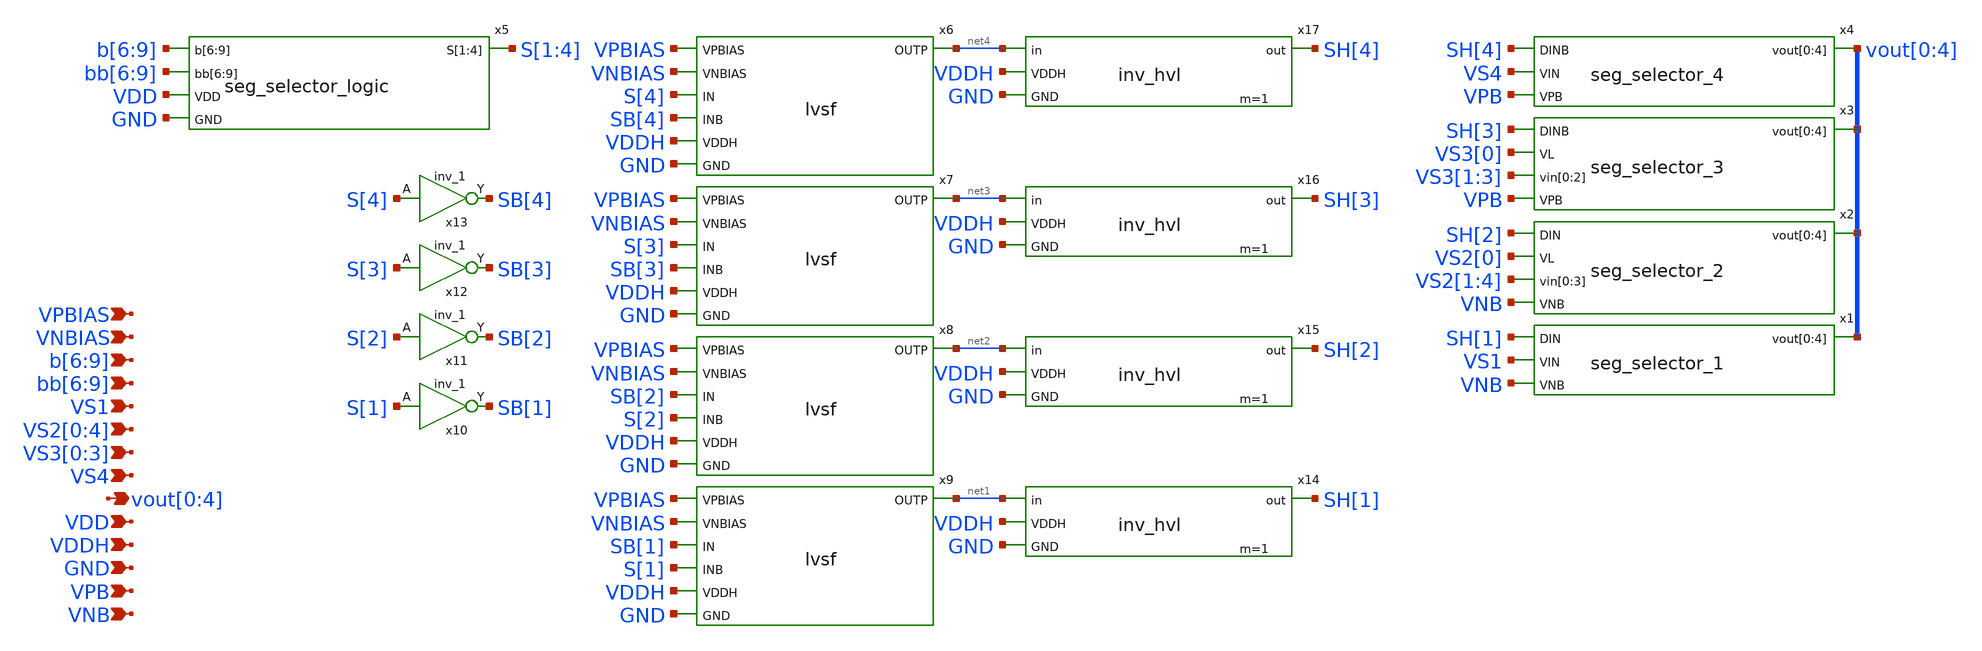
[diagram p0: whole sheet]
** sch_path: xschem/seg_selector.sch
**.subckt seg_selector vout[0],vout[1],vout[2],vout[3],vout[4] VNB VPB b[6],b[7],b[8],b[9] VS1
*+ VS2[0],VS2[1],VS2[2],VS2[3],VS2[4] VS3[0],VS3[1],VS3[2],VS3[3] VS4 bb[6],bb[7],bb[8],bb[9] GND VDD VPBIAS VNBIAS VDDH
*.opin vout[0],vout[1],vout[2],vout[3],vout[4]
*.ipin VNB
*.ipin VPB
*.ipin b[6],b[7],b[8],b[9]
*.ipin VS1
*.ipin VS2[0],VS2[1],VS2[2],VS2[3],VS2[4]
*.ipin VS3[0],VS3[1],VS3[2],VS3[3]
*.ipin VS4
*.ipin bb[6],bb[7],bb[8],bb[9]
*.ipin GND
*.ipin VDD
*.ipin VPBIAS
*.ipin VNBIAS
*.ipin VDDH
x1 SH[1] VS1 vout[0] vout[1] vout[2] vout[3] vout[4] VNB seg_selector_1
x2 SH[2] VS2[0] VS2[1] VS2[2] VS2[3] VS2[4] vout[0] vout[1] vout[2] vout[3] vout[4] VNB
+ seg_selector_2
x3 SH[3] VS3[0] VS3[1] VS3[2] VS3[3] vout[0] vout[1] vout[2] vout[3] vout[4] VPB seg_selector_3
x4 SH[4] VS4 vout[0] vout[1] vout[2] vout[3] vout[4] VPB seg_selector_4
x5 b[6] b[7] b[8] b[9] bb[6] bb[7] bb[8] bb[9] S[1] S[2] S[3] S[4] VDD GND seg_selector_logic
x6 VPBIAS VNBIAS S[4] SB[4] net4 VDDH GND lvsf
x7 VPBIAS VNBIAS S[3] SB[3] net3 VDDH GND lvsf
x8 VPBIAS VNBIAS SB[2] S[2] net2 VDDH GND lvsf
x9 VPBIAS VNBIAS SB[1] S[1] net1 VDDH GND lvsf
x10 S[1] GND GND VDD VDD SB[1] sky130_fd_sc_hd__inv_1
x11 S[2] GND GND VDD VDD SB[2] sky130_fd_sc_hd__inv_1
x12 S[3] GND GND VDD VDD SB[3] sky130_fd_sc_hd__inv_1
x13 S[4] GND GND VDD VDD SB[4] sky130_fd_sc_hd__inv_1
x14 net1 SH[1] VDDH GND inv_hvl m=1
x15 net2 SH[2] VDDH GND inv_hvl m=1
x16 net3 SH[3] VDDH GND inv_hvl m=1
x17 net4 SH[4] VDDH GND inv_hvl m=1
**.ends

* expanding   symbol:  seg_selector_1.sym # of pins=4
** sym_path: xschem/seg_selector_1.sym
** sch_path: xschem/seg_selector_1.sch
.subckt seg_selector_1 DIN VIN vout[0] vout[1] vout[2] vout[3] vout[4] VNB
*.opin vout[0],vout[1],vout[2],vout[3],vout[4]
*.ipin VNB
*.ipin DIN
*.ipin VIN
.param wp=0.42 wn=0.42 l=0.5

XM1 vout[0] DIN VIN VNB sky130_fd_pr__nfet_g5v0d10v5 L=l W=wn nf=1 ad='int((nf+1)/2) * W/nf * 0.29' as='int((nf+2)/2) * W/nf * 0.29'
+ pd='2*int((nf+1)/2) * (W/nf + 0.29)' ps='2*int((nf+2)/2) * (W/nf + 0.29)' nrd='0.29 / W' nrs='0.29 / W'
+ sa=0 sb=0 sd=0 mult=1 m=1
XM2 vout[1] DIN VIN VNB sky130_fd_pr__nfet_g5v0d10v5 L=l W=wn nf=1 ad='int((nf+1)/2) * W/nf * 0.29' as='int((nf+2)/2) * W/nf * 0.29'
+ pd='2*int((nf+1)/2) * (W/nf + 0.29)' ps='2*int((nf+2)/2) * (W/nf + 0.29)' nrd='0.29 / W' nrs='0.29 / W'
+ sa=0 sb=0 sd=0 mult=1 m=1
XM3 vout[2] DIN VIN VNB sky130_fd_pr__nfet_g5v0d10v5 L=l W=wn nf=1 ad='int((nf+1)/2) * W/nf * 0.29' as='int((nf+2)/2) * W/nf * 0.29'
+ pd='2*int((nf+1)/2) * (W/nf + 0.29)' ps='2*int((nf+2)/2) * (W/nf + 0.29)' nrd='0.29 / W' nrs='0.29 / W'
+ sa=0 sb=0 sd=0 mult=1 m=1
XM4 vout[3] DIN VIN VNB sky130_fd_pr__nfet_g5v0d10v5 L=l W=wn nf=1 ad='int((nf+1)/2) * W/nf * 0.29' as='int((nf+2)/2) * W/nf * 0.29'
+ pd='2*int((nf+1)/2) * (W/nf + 0.29)' ps='2*int((nf+2)/2) * (W/nf + 0.29)' nrd='0.29 / W' nrs='0.29 / W'
+ sa=0 sb=0 sd=0 mult=1 m=1
XM5 vout[4] DIN VIN VNB sky130_fd_pr__nfet_g5v0d10v5 L=l W=wn nf=1 ad='int((nf+1)/2) * W/nf * 0.29' as='int((nf+2)/2) * W/nf * 0.29'
+ pd='2*int((nf+1)/2) * (W/nf + 0.29)' ps='2*int((nf+2)/2) * (W/nf + 0.29)' nrd='0.29 / W' nrs='0.29 / W'
+ sa=0 sb=0 sd=0 mult=1 m=1
.ends


* expanding   symbol:  seg_selector_2.sym # of pins=5
** sym_path: xschem/seg_selector_2.sym
** sch_path: xschem/seg_selector_2.sch
.subckt seg_selector_2 DIN VL vin[0] vin[1] vin[2] vin[3] vout[0] vout[1] vout[2] vout[3] vout[4]
+ VNB
*.opin vout[0],vout[1],vout[2],vout[3],vout[4]
*.ipin VNB
*.ipin DIN
*.ipin vin[0],vin[1],vin[2],vin[3]
*.ipin VL
.param wp=0.42 wn=0.42 l=0.5

XM1 vout[0] DIN VL VNB sky130_fd_pr__nfet_g5v0d10v5 L=l W=wn nf=1 ad='int((nf+1)/2) * W/nf * 0.29' as='int((nf+2)/2) * W/nf * 0.29'
+ pd='2*int((nf+1)/2) * (W/nf + 0.29)' ps='2*int((nf+2)/2) * (W/nf + 0.29)' nrd='0.29 / W' nrs='0.29 / W'
+ sa=0 sb=0 sd=0 mult=1 m=1
XM2 vout[1] DIN vin[0] VNB sky130_fd_pr__nfet_g5v0d10v5 L=l W=wn nf=1 ad='int((nf+1)/2) * W/nf * 0.29'
+ as='int((nf+2)/2) * W/nf * 0.29' pd='2*int((nf+1)/2) * (W/nf + 0.29)' ps='2*int((nf+2)/2) * (W/nf + 0.29)'
+ nrd='0.29 / W' nrs='0.29 / W' sa=0 sb=0 sd=0 mult=1 m=1
XM3 vout[2] DIN vin[1] VNB sky130_fd_pr__nfet_g5v0d10v5 L=l W=wn nf=1 ad='int((nf+1)/2) * W/nf * 0.29'
+ as='int((nf+2)/2) * W/nf * 0.29' pd='2*int((nf+1)/2) * (W/nf + 0.29)' ps='2*int((nf+2)/2) * (W/nf + 0.29)'
+ nrd='0.29 / W' nrs='0.29 / W' sa=0 sb=0 sd=0 mult=1 m=1
XM4 vout[3] DIN vin[2] VNB sky130_fd_pr__nfet_g5v0d10v5 L=l W=wn nf=1 ad='int((nf+1)/2) * W/nf * 0.29'
+ as='int((nf+2)/2) * W/nf * 0.29' pd='2*int((nf+1)/2) * (W/nf + 0.29)' ps='2*int((nf+2)/2) * (W/nf + 0.29)'
+ nrd='0.29 / W' nrs='0.29 / W' sa=0 sb=0 sd=0 mult=1 m=1
XM5 vout[4] DIN vin[3] VNB sky130_fd_pr__nfet_g5v0d10v5 L=l W=wn nf=1 ad='int((nf+1)/2) * W/nf * 0.29'
+ as='int((nf+2)/2) * W/nf * 0.29' pd='2*int((nf+1)/2) * (W/nf + 0.29)' ps='2*int((nf+2)/2) * (W/nf + 0.29)'
+ nrd='0.29 / W' nrs='0.29 / W' sa=0 sb=0 sd=0 mult=1 m=1
.ends


* expanding   symbol:  seg_selector_3.sym # of pins=5
** sym_path: xschem/seg_selector_3.sym
** sch_path: xschem/seg_selector_3.sch
.subckt seg_selector_3 DINB VL vin[0] vin[1] vin[2] vout[0] vout[1] vout[2] vout[3] vout[4] VPB
*.opin vout[0],vout[1],vout[2],vout[3],vout[4]
*.ipin VPB
*.ipin DINB
*.ipin vin[0],vin[1],vin[2]
*.ipin VL
.param wp=0.42 wn=0.42 l=0.5

XM1 vout[0] DINB VL VPB sky130_fd_pr__pfet_g5v0d10v5 L=l W=wp nf=1 ad='int((nf+1)/2) * W/nf * 0.29' as='int((nf+2)/2) * W/nf * 0.29'
+ pd='2*int((nf+1)/2) * (W/nf + 0.29)' ps='2*int((nf+2)/2) * (W/nf + 0.29)' nrd='0.29 / W' nrs='0.29 / W'
+ sa=0 sb=0 sd=0 mult=1 m=1
XM2 vout[1] DINB VL VPB sky130_fd_pr__pfet_g5v0d10v5 L=l W=wp nf=1 ad='int((nf+1)/2) * W/nf * 0.29' as='int((nf+2)/2) * W/nf * 0.29'
+ pd='2*int((nf+1)/2) * (W/nf + 0.29)' ps='2*int((nf+2)/2) * (W/nf + 0.29)' nrd='0.29 / W' nrs='0.29 / W'
+ sa=0 sb=0 sd=0 mult=1 m=1
XM3 vout[2] DINB vin[0] VPB sky130_fd_pr__pfet_g5v0d10v5 L=l W=wp nf=1 ad='int((nf+1)/2) * W/nf * 0.29'
+ as='int((nf+2)/2) * W/nf * 0.29' pd='2*int((nf+1)/2) * (W/nf + 0.29)' ps='2*int((nf+2)/2) * (W/nf + 0.29)'
+ nrd='0.29 / W' nrs='0.29 / W' sa=0 sb=0 sd=0 mult=1 m=1
XM4 vout[3] DINB vin[1] VPB sky130_fd_pr__pfet_g5v0d10v5 L=l W=wp nf=1 ad='int((nf+1)/2) * W/nf * 0.29'
+ as='int((nf+2)/2) * W/nf * 0.29' pd='2*int((nf+1)/2) * (W/nf + 0.29)' ps='2*int((nf+2)/2) * (W/nf + 0.29)'
+ nrd='0.29 / W' nrs='0.29 / W' sa=0 sb=0 sd=0 mult=1 m=1
XM5 vout[4] DINB vin[2] VPB sky130_fd_pr__pfet_g5v0d10v5 L=l W=wp nf=1 ad='int((nf+1)/2) * W/nf * 0.29'
+ as='int((nf+2)/2) * W/nf * 0.29' pd='2*int((nf+1)/2) * (W/nf + 0.29)' ps='2*int((nf+2)/2) * (W/nf + 0.29)'
+ nrd='0.29 / W' nrs='0.29 / W' sa=0 sb=0 sd=0 mult=1 m=1
.ends


* expanding   symbol:  seg_selector_4.sym # of pins=4
** sym_path: xschem/seg_selector_4.sym
** sch_path: xschem/seg_selector_4.sch
.subckt seg_selector_4 DINB VIN vout[0] vout[1] vout[2] vout[3] vout[4] VPB
*.opin vout[0],vout[1],vout[2],vout[3],vout[4]
*.ipin VPB
*.ipin DINB
*.ipin VIN
.param wp=0.42 wn=0.42 l=0.5

XM1 vout[0] DINB VIN VPB sky130_fd_pr__pfet_g5v0d10v5 L=l W=wp nf=1 ad='int((nf+1)/2) * W/nf * 0.29'
+ as='int((nf+2)/2) * W/nf * 0.29' pd='2*int((nf+1)/2) * (W/nf + 0.29)' ps='2*int((nf+2)/2) * (W/nf + 0.29)'
+ nrd='0.29 / W' nrs='0.29 / W' sa=0 sb=0 sd=0 mult=1 m=1
XM2 vout[1] DINB VIN VPB sky130_fd_pr__pfet_g5v0d10v5 L=l W=wp nf=1 ad='int((nf+1)/2) * W/nf * 0.29'
+ as='int((nf+2)/2) * W/nf * 0.29' pd='2*int((nf+1)/2) * (W/nf + 0.29)' ps='2*int((nf+2)/2) * (W/nf + 0.29)'
+ nrd='0.29 / W' nrs='0.29 / W' sa=0 sb=0 sd=0 mult=1 m=1
XM3 vout[2] DINB VIN VPB sky130_fd_pr__pfet_g5v0d10v5 L=l W=wp nf=1 ad='int((nf+1)/2) * W/nf * 0.29'
+ as='int((nf+2)/2) * W/nf * 0.29' pd='2*int((nf+1)/2) * (W/nf + 0.29)' ps='2*int((nf+2)/2) * (W/nf + 0.29)'
+ nrd='0.29 / W' nrs='0.29 / W' sa=0 sb=0 sd=0 mult=1 m=1
XM4 vout[3] DINB VIN VPB sky130_fd_pr__pfet_g5v0d10v5 L=l W=wp nf=1 ad='int((nf+1)/2) * W/nf * 0.29'
+ as='int((nf+2)/2) * W/nf * 0.29' pd='2*int((nf+1)/2) * (W/nf + 0.29)' ps='2*int((nf+2)/2) * (W/nf + 0.29)'
+ nrd='0.29 / W' nrs='0.29 / W' sa=0 sb=0 sd=0 mult=1 m=1
XM5 vout[4] DINB VIN VPB sky130_fd_pr__pfet_g5v0d10v5 L=l W=wp nf=1 ad='int((nf+1)/2) * W/nf * 0.29'
+ as='int((nf+2)/2) * W/nf * 0.29' pd='2*int((nf+1)/2) * (W/nf + 0.29)' ps='2*int((nf+2)/2) * (W/nf + 0.29)'
+ nrd='0.29 / W' nrs='0.29 / W' sa=0 sb=0 sd=0 mult=1 m=1
.ends


* expanding   symbol:  seg_selector_logic.sym # of pins=5
** sym_path: xschem/seg_selector_logic.sym
** sch_path: xschem/seg_selector_logic.sch
.subckt seg_selector_logic b[6] b[7] b[8] b[9] bb[6] bb[7] bb[8] bb[9] S[1] S[2] S[3] S[4] VDD GND
*.ipin b[6],b[7],b[8],b[9]
*.opin S[1],S[2],S[3],S[4]
*.ipin GND
*.ipin VDD
*.ipin bb[6],bb[7],bb[8],bb[9]
x1 bb[6] bb[7] bb[8] bb[9] S[1] VDD GND seg_selector_1_logic
x2 b[6] b[7] b[8] b[9] bb[6] bb[7] bb[8] bb[9] S[2] VDD GND seg_selector_2_logic
x3 b[6] b[7] b[8] b[9] bb[6] bb[7] S[3] VDD GND seg_selector_3_logic
x4 b[6] b[7] b[8] b[9] S[4] VDD GND seg_selector_4_logic
.ends


* expanding   symbol:  lvsf.sym # of pins=7
** sym_path: xschem/lvsf.sym
** sch_path: xschem/lvsf.sch
.subckt lvsf VPBIAS VNBIAS IN INB OUTP VDDH GND
*.ipin IN
*.ipin INB
*.opin OUTP
*.ipin VDDH
*.ipin GND
*.ipin VPBIAS
*.ipin VNBIAS
Vmeas net1 net2 0
.save i(vmeas)
XM13 net6 IN GND GND sky130_fd_pr__nfet_01v8 L=0.15 W=3 nf=1 ad='int((nf+1)/2) * W/nf * 0.29' as='int((nf+2)/2) * W/nf * 0.29'
+ pd='2*int((nf+1)/2) * (W/nf + 0.29)' ps='2*int((nf+2)/2) * (W/nf + 0.29)' nrd='0.29 / W' nrs='0.29 / W'
+ sa=0 sb=0 sd=0 mult=1 m=1
XM1 net3 VPBIAS VDDH VDDH sky130_fd_pr__pfet_g5v0d10v5 L=0.8 W=1 nf=1 ad='int((nf+1)/2) * W/nf * 0.29'
+ as='int((nf+2)/2) * W/nf * 0.29' pd='2*int((nf+1)/2) * (W/nf + 0.29)' ps='2*int((nf+2)/2) * (W/nf + 0.29)'
+ nrd='0.29 / W' nrs='0.29 / W' sa=0 sb=0 sd=0 mult=1 m=1
XM2 net1 VPBIAS VDDH VDDH sky130_fd_pr__pfet_g5v0d10v5 L=0.8 W=1 nf=1 ad='int((nf+1)/2) * W/nf * 0.29'
+ as='int((nf+2)/2) * W/nf * 0.29' pd='2*int((nf+1)/2) * (W/nf + 0.29)' ps='2*int((nf+2)/2) * (W/nf + 0.29)'
+ nrd='0.29 / W' nrs='0.29 / W' sa=0 sb=0 sd=0 mult=1 m=1
XM3 OUTPB OUTP net4 VDDH sky130_fd_pr__pfet_g5v0d10v5 L=0.8 W=1 nf=1 ad='int((nf+1)/2) * W/nf * 0.29'
+ as='int((nf+2)/2) * W/nf * 0.29' pd='2*int((nf+1)/2) * (W/nf + 0.29)' ps='2*int((nf+2)/2) * (W/nf + 0.29)'
+ nrd='0.29 / W' nrs='0.29 / W' sa=0 sb=0 sd=0 mult=1 m=1
XM4 OUTP OUTPB net2 VDDH sky130_fd_pr__pfet_g5v0d10v5 L=0.8 W=1 nf=1 ad='int((nf+1)/2) * W/nf * 0.29'
+ as='int((nf+2)/2) * W/nf * 0.29' pd='2*int((nf+1)/2) * (W/nf + 0.29)' ps='2*int((nf+2)/2) * (W/nf + 0.29)'
+ nrd='0.29 / W' nrs='0.29 / W' sa=0 sb=0 sd=0 mult=1 m=1
XM5 OUTPB VNBIAS n1 GND sky130_fd_pr__nfet_g5v0d10v5 L=1 W=1 nf=1 ad='int((nf+1)/2) * W/nf * 0.29' as='int((nf+2)/2) * W/nf * 0.29'
+ pd='2*int((nf+1)/2) * (W/nf + 0.29)' ps='2*int((nf+2)/2) * (W/nf + 0.29)' nrd='0.29 / W' nrs='0.29 / W'
+ sa=0 sb=0 sd=0 mult=1 m=1
XM6 OUTP VNBIAS n2 GND sky130_fd_pr__nfet_g5v0d10v5 L=1 W=1 nf=1 ad='int((nf+1)/2) * W/nf * 0.29' as='int((nf+2)/2) * W/nf * 0.29'
+ pd='2*int((nf+1)/2) * (W/nf + 0.29)' ps='2*int((nf+2)/2) * (W/nf + 0.29)' nrd='0.29 / W' nrs='0.29 / W'
+ sa=0 sb=0 sd=0 mult=1 m=1
Vmeas1 net3 net4 0
.save i(vmeas1)
XM7 net5 INB GND GND sky130_fd_pr__nfet_01v8 L=0.15 W=3 nf=1 ad='int((nf+1)/2) * W/nf * 0.29' as='int((nf+2)/2) * W/nf * 0.29'
+ pd='2*int((nf+1)/2) * (W/nf + 0.29)' ps='2*int((nf+2)/2) * (W/nf + 0.29)' nrd='0.29 / W' nrs='0.29 / W'
+ sa=0 sb=0 sd=0 mult=1 m=1
Vmeas2 n2 net5 0
.save i(vmeas2)
Vmeas3 n1 net6 0
.save i(vmeas3)
.ends


* expanding   symbol:  inv_hvl.sym # of pins=4
** sym_path: xschem/inv_hvl.sym
** sch_path: xschem/inv_hvl.sch
.subckt inv_hvl in out VDDH GND
*.opin out
*.ipin VDDH
*.ipin GND
*.ipin in
.param wp=0.84 wn=0.42 l=0.5
XM1 out in VDDH VDDH sky130_fd_pr__pfet_g5v0d10v5 L=l W=wp nf=1 ad='int((nf+1)/2) * W/nf * 0.29' as='int((nf+2)/2) * W/nf * 0.29'
+ pd='2*int((nf+1)/2) * (W/nf + 0.29)' ps='2*int((nf+2)/2) * (W/nf + 0.29)' nrd='0.29 / W' nrs='0.29 / W'
+ sa=0 sb=0 sd=0 mult=m m=m
XM2 out in GND GND sky130_fd_pr__nfet_g5v0d10v5 L=l W=wn nf=1 ad='int((nf+1)/2) * W/nf * 0.29' as='int((nf+2)/2) * W/nf * 0.29'
+ pd='2*int((nf+1)/2) * (W/nf + 0.29)' ps='2*int((nf+2)/2) * (W/nf + 0.29)' nrd='0.29 / W' nrs='0.29 / W'
+ sa=0 sb=0 sd=0 mult=m m=m
.ends


* expanding   symbol:  seg_selector_1_logic.sym # of pins=4
** sym_path: xschem/seg_selector_1_logic.sym
** sch_path: xschem/seg_selector_1_logic.sch
.subckt seg_selector_1_logic bb[6] bb[7] bb[8] bb[9] S VDD GND
*.opin S
*.ipin GND
*.ipin VDD
*.ipin bb[6],bb[7],bb[8],bb[9]
x1 bb[9] bb[8] GND GND VDD VDD net2 sky130_fd_sc_hd__nand2_1
x3 net2 net1 GND GND VDD VDD S sky130_fd_sc_hd__nor2_1
x2 bb[7] bb[6] GND GND VDD VDD net1 sky130_fd_sc_hd__nand2_1
.ends


* expanding   symbol:  seg_selector_2_logic.sym # of pins=5
** sym_path: xschem/seg_selector_2_logic.sym
** sch_path: xschem/seg_selector_2_logic.sch
.subckt seg_selector_2_logic b[6] b[7] b[8] b[9] bb[6] bb[7] bb[8] bb[9] S VDD GND
*.ipin b[6],b[7],b[8],b[9]
*.opin S
*.ipin GND
*.ipin VDD
*.ipin bb[6],bb[7],bb[8],bb[9]
x1 bb[9] b[6] GND GND VDD VDD n1 sky130_fd_sc_hd__nand2_1
x2 bb[9] b[7] GND GND VDD VDD n2 sky130_fd_sc_hd__nand2_1
x3 b[9] bb[8] GND GND VDD VDD n3 sky130_fd_sc_hd__nand2_1
x5 b[8] bb[7] bb[6] GND GND VDD VDD n4 sky130_fd_sc_hd__nand3_1
x4 n4 n3 n2 n1 GND GND VDD VDD S sky130_fd_sc_hd__nand4_1
.ends


* expanding   symbol:  seg_selector_3_logic.sym # of pins=5
** sym_path: xschem/seg_selector_3_logic.sym
** sch_path: xschem/seg_selector_3_logic.sch
.subckt seg_selector_3_logic b[6] b[7] b[8] b[9] bb[6] bb[7] S VDD GND
*.opin S
*.ipin GND
*.ipin VDD
*.ipin b[6],b[7],b[8],b[9]
*.ipin bb[6],bb[7]
x2 b[9] b[8] b[7] bb[6] GND GND VDD VDD net1 sky130_fd_sc_hd__nand4_1
x1 b[9] b[8] bb[7] b[6] GND GND VDD VDD net2 sky130_fd_sc_hd__nand4_1
x3 net2 net1 GND GND VDD VDD S sky130_fd_sc_hd__nand2_1
.ends


* expanding   symbol:  seg_selector_4_logic.sym # of pins=4
** sym_path: xschem/seg_selector_4_logic.sym
** sch_path: xschem/seg_selector_4_logic.sch
.subckt seg_selector_4_logic b[6] b[7] b[8] b[9] S VDD GND
*.opin S
*.ipin GND
*.ipin VDD
*.ipin b[6],b[7],b[8],b[9]
x1 b[9] b[8] GND GND VDD VDD net1 sky130_fd_sc_hd__nand2_1
x2 b[7] b[6] GND GND VDD VDD net2 sky130_fd_sc_hd__nand2_1
x3 net1 net2 GND GND VDD VDD S sky130_fd_sc_hd__nor2_1
.ends

.end
